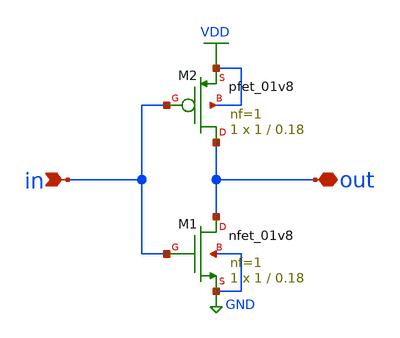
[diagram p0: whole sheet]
** sch_path: xschem/HW4_RAM_readout/inv/inv_1.sch
**.subckt inv_1 in out
*.ipin in
*.iopin out
XM1 out in GND GND sky130_fd_pr__nfet_01v8 L=0.18 W=1 nf=1 ad='int((nf+1)/2) * W/nf * 0.29' as='int((nf+2)/2) * W/nf * 0.29'
+ pd='2*int((nf+1)/2) * (W/nf + 0.29)' ps='2*int((nf+2)/2) * (W/nf + 0.29)' nrd='0.29 / W' nrs='0.29 / W'
+ sa=0 sb=0 sd=0 mult=1 m=1
XM2 out in VDD VDD sky130_fd_pr__pfet_01v8 L=0.18 W=1 nf=1 ad='int((nf+1)/2) * W/nf * 0.29' as='int((nf+2)/2) * W/nf * 0.29'
+ pd='2*int((nf+1)/2) * (W/nf + 0.29)' ps='2*int((nf+2)/2) * (W/nf + 0.29)' nrd='0.29 / W' nrs='0.29 / W'
+ sa=0 sb=0 sd=0 mult=1 m=1
**.ends
.GLOBAL VDD
.GLOBAL GND
.end
